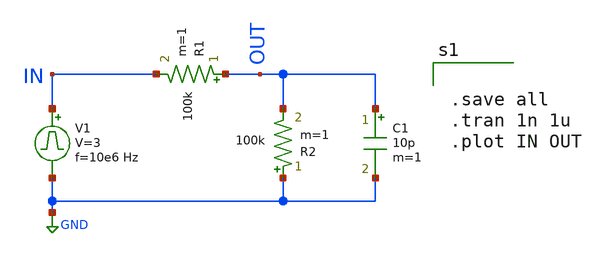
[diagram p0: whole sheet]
** sch_path: test_sch.sch
**.subckt test_sch
V1 IN GND pulse 0 3 '0.495/ 10e6 ' '0.01/10e6 ' '0.01/10e6 ' '0.49/10e6 ' '1/10e6 '
R1 OUT IN 100k m=1
R2 GND OUT 100k m=1
C1 OUT GND 10p m=1
**** begin user architecture code


.save all
.tran 1n 1u
.plot IN OUT


**** end user architecture code
**.ends
.GLOBAL GND
.end
